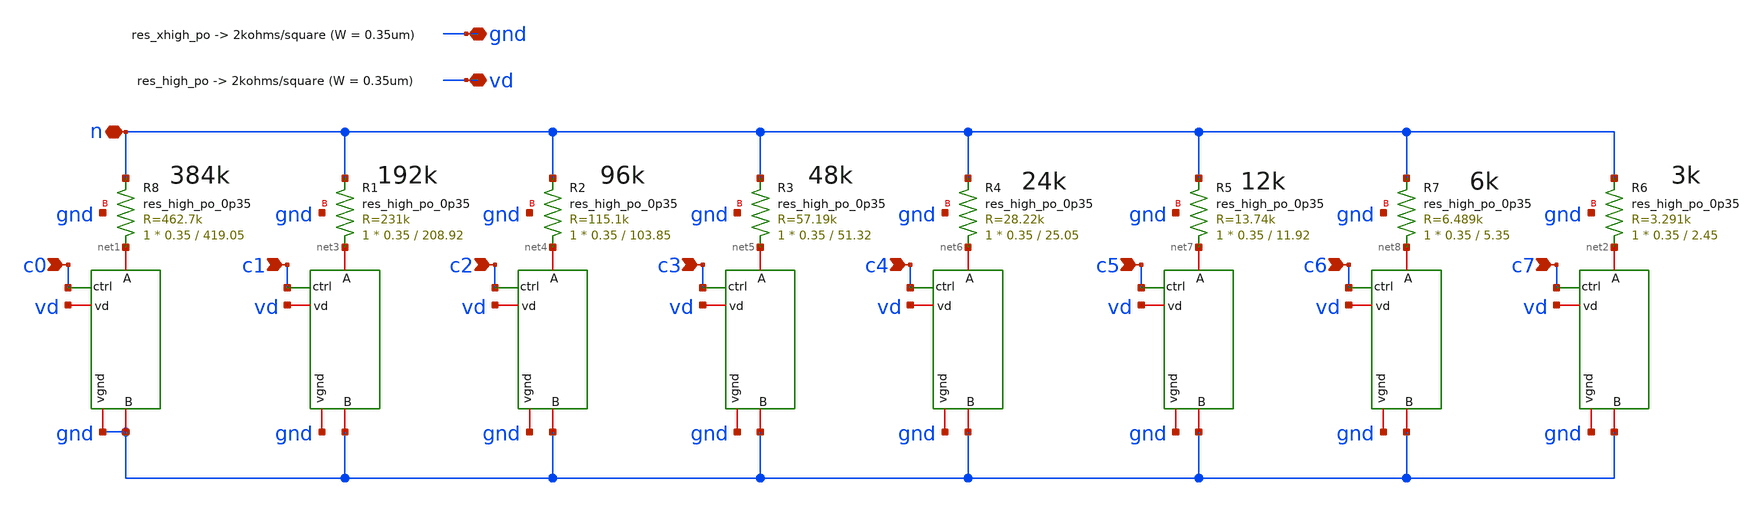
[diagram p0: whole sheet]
** sch_path: xschem/digipot.sch
**.subckt digipot c0 c1 c2 c3 c4 c5 c6 c7 gnd vd n
*.ipin c0
*.ipin c1
*.ipin c2
*.ipin c3
*.ipin c4
*.ipin c5
*.ipin c6
*.ipin c7
*.iopin gnd
*.iopin vd
*.iopin n
x1 vd c0 gnd net1 gnd tg
XR6 net2 n gnd sky130_fd_pr__res_high_po_0p35 L=2.45 mult=1 m=1
x2 vd c1 gnd net3 gnd tg
x3 vd c2 gnd net4 gnd tg
x4 vd c3 gnd net5 gnd tg
x5 vd c4 gnd net6 gnd tg
x6 vd c5 gnd net7 gnd tg
x7 vd c6 gnd net8 gnd tg
x8 vd c7 gnd net2 gnd tg
XR7 net8 n gnd sky130_fd_pr__res_high_po_0p35 L=5.35 mult=1 m=1
XR5 net7 n gnd sky130_fd_pr__res_high_po_0p35 L=11.92 mult=1 m=1
XR4 net6 n gnd sky130_fd_pr__res_high_po_0p35 L=25.05 mult=1 m=1
XR3 net5 n gnd sky130_fd_pr__res_high_po_0p35 L=51.32 mult=1 m=1
XR2 net4 n gnd sky130_fd_pr__res_high_po_0p35 L=103.85 mult=1 m=1
XR1 net3 n gnd sky130_fd_pr__res_high_po_0p35 L=208.92 mult=1 m=1
XR8 net1 n gnd sky130_fd_pr__res_high_po_0p35 L=419.05 mult=1 m=1
**.ends

* expanding   symbol:  /foss/designs/tg.sym # of pins=5
** sym_path: xschem/tg.sym
** sch_path: xschem/tg.sch
.subckt tg vd ctrl vgnd A B
*.iopin B
*.iopin A
*.iopin vgnd
*.iopin vd
*.ipin ctrl
x1 vd ctrl nctrl vgnd inverter
XM1 A ctrl B vgnd sky130_fd_pr__nfet_01v8 L=0.15 W=10 nf=1 ad='int((nf+1)/2) * W/nf * 0.29' as='int((nf+2)/2) * W/nf * 0.29'
+ pd='2*int((nf+1)/2) * (W/nf + 0.29)' ps='2*int((nf+2)/2) * (W/nf + 0.29)' nrd='0.29 / W' nrs='0.29 / W'
+ sa=0 sb=0 sd=0 mult=1 m=1
XM2 A nctrl B vd sky130_fd_pr__pfet_01v8 L=0.15 W=30 nf=1 ad='int((nf+1)/2) * W/nf * 0.29' as='int((nf+2)/2) * W/nf * 0.29'
+ pd='2*int((nf+1)/2) * (W/nf + 0.29)' ps='2*int((nf+2)/2) * (W/nf + 0.29)' nrd='0.29 / W' nrs='0.29 / W'
+ sa=0 sb=0 sd=0 mult=1 m=1
.ends


* expanding   symbol:  /foss/designs/inverter/xschem_files/inverter.sym # of pins=4
** sym_path: /foss/designs/inverter/xschem_files/inverter.sym
** sch_path: /foss/designs/inverter/xschem_files/inverter.sch
.subckt inverter vd in out gnd
*.ipin in
*.opin out
*.iopin vd
*.iopin gnd
XN0 out in gnd gnd sky130_fd_pr__nfet_01v8 L=0.15 W=1 nf=1 ad='int((nf+1)/2) * W/nf * 0.29' as='int((nf+2)/2) * W/nf * 0.29'
+ pd='2*int((nf+1)/2) * (W/nf + 0.29)' ps='2*int((nf+2)/2) * (W/nf + 0.29)' nrd='0.29 / W' nrs='0.29 / W'
+ sa=0 sb=0 sd=0 mult=1 m=1
XP0 out in vd vd sky130_fd_pr__pfet_01v8 L=0.15 W=3 nf=1 ad='int((nf+1)/2) * W/nf * 0.29' as='int((nf+2)/2) * W/nf * 0.29'
+ pd='2*int((nf+1)/2) * (W/nf + 0.29)' ps='2*int((nf+2)/2) * (W/nf + 0.29)' nrd='0.29 / W' nrs='0.29 / W'
+ sa=0 sb=0 sd=0 mult=1 m=1
.ends

.end
